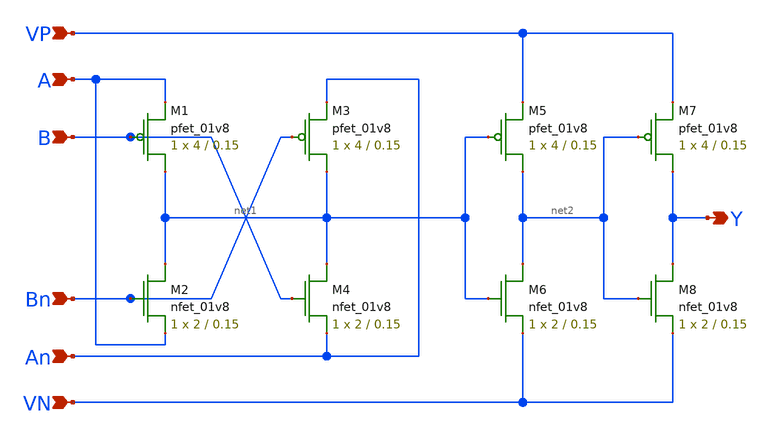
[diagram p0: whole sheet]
** sch_path: Mixed-Signal TRNG/xschem/xor.sch
**.subckt xor B Bn A An Y VP VN
*.ipin B
*.ipin Bn
*.ipin A
*.ipin An
*.opin Y
*.ipin VP
*.ipin VN
XM3 net1 Bn An VP sky130_fd_pr__pfet_01v8 L=0.15 W=4 nf=1 ad='int((nf+1)/2) * W/nf * 0.29' as='int((nf+2)/2) * W/nf * 0.29'
+ pd='2*int((nf+1)/2) * (W/nf + 0.29)' ps='2*int((nf+2)/2) * (W/nf + 0.29)' nrd='0.29 / W' nrs='0.29 / W'
+ sa=0 sb=0 sd=0 mult=1 m=1
XM4 net1 B An VN sky130_fd_pr__nfet_01v8 L=0.15 W=2 nf=1 ad='int((nf+1)/2) * W/nf * 0.29' as='int((nf+2)/2) * W/nf * 0.29'
+ pd='2*int((nf+1)/2) * (W/nf + 0.29)' ps='2*int((nf+2)/2) * (W/nf + 0.29)' nrd='0.29 / W' nrs='0.29 / W'
+ sa=0 sb=0 sd=0 mult=1 m=1
XM5 net2 net1 VP VP sky130_fd_pr__pfet_01v8 L=0.15 W=4 nf=1 ad='int((nf+1)/2) * W/nf * 0.29' as='int((nf+2)/2) * W/nf * 0.29'
+ pd='2*int((nf+1)/2) * (W/nf + 0.29)' ps='2*int((nf+2)/2) * (W/nf + 0.29)' nrd='0.29 / W' nrs='0.29 / W'
+ sa=0 sb=0 sd=0 mult=1 m=1
XM6 net2 net1 VN VN sky130_fd_pr__nfet_01v8 L=0.15 W=2 nf=1 ad='int((nf+1)/2) * W/nf * 0.29' as='int((nf+2)/2) * W/nf * 0.29'
+ pd='2*int((nf+1)/2) * (W/nf + 0.29)' ps='2*int((nf+2)/2) * (W/nf + 0.29)' nrd='0.29 / W' nrs='0.29 / W'
+ sa=0 sb=0 sd=0 mult=1 m=1
XM1 net1 B A VP sky130_fd_pr__pfet_01v8 L=0.15 W=4 nf=1 ad='int((nf+1)/2) * W/nf * 0.29' as='int((nf+2)/2) * W/nf * 0.29'
+ pd='2*int((nf+1)/2) * (W/nf + 0.29)' ps='2*int((nf+2)/2) * (W/nf + 0.29)' nrd='0.29 / W' nrs='0.29 / W'
+ sa=0 sb=0 sd=0 mult=1 m=1
XM2 net1 Bn A VN sky130_fd_pr__nfet_01v8 L=0.15 W=2 nf=1 ad='int((nf+1)/2) * W/nf * 0.29' as='int((nf+2)/2) * W/nf * 0.29'
+ pd='2*int((nf+1)/2) * (W/nf + 0.29)' ps='2*int((nf+2)/2) * (W/nf + 0.29)' nrd='0.29 / W' nrs='0.29 / W'
+ sa=0 sb=0 sd=0 mult=1 m=1
XM7 Y net2 VP VP sky130_fd_pr__pfet_01v8 L=0.15 W=4 nf=1 ad='int((nf+1)/2) * W/nf * 0.29' as='int((nf+2)/2) * W/nf * 0.29'
+ pd='2*int((nf+1)/2) * (W/nf + 0.29)' ps='2*int((nf+2)/2) * (W/nf + 0.29)' nrd='0.29 / W' nrs='0.29 / W'
+ sa=0 sb=0 sd=0 mult=1 m=1
XM8 Y net2 VN VN sky130_fd_pr__nfet_01v8 L=0.15 W=2 nf=1 ad='int((nf+1)/2) * W/nf * 0.29' as='int((nf+2)/2) * W/nf * 0.29'
+ pd='2*int((nf+1)/2) * (W/nf + 0.29)' ps='2*int((nf+2)/2) * (W/nf + 0.29)' nrd='0.29 / W' nrs='0.29 / W'
+ sa=0 sb=0 sd=0 mult=1 m=1
**.ends
.end
